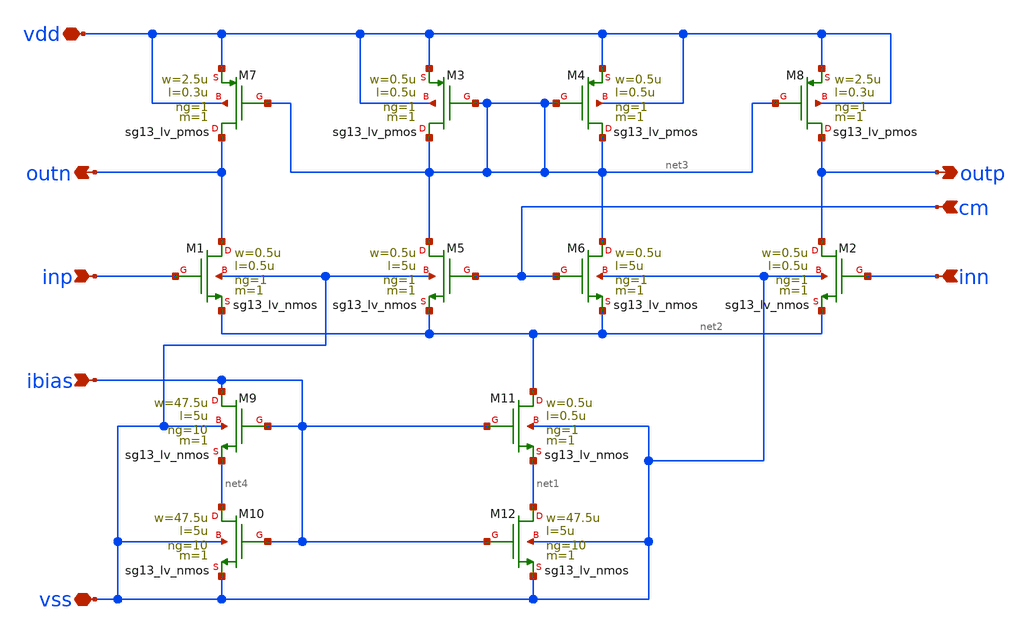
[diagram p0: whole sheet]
** sch_path: 3_Real_Cir/ota_gm_100u.sch
**.subckt ota_gm_100u inn outp outn vdd cm vss ibias inp
*.ipin inn
*.opin outp
*.opin outn
*.iopin vdd
*.ipin cm
*.iopin vss
*.ipin ibias
*.ipin inp
XM3 net3 net3 vdd vdd sg13_lv_pmos w=0.5u l=0.5u ng=1 m=1 mm_ok=1
XM4 net3 net3 vdd vdd sg13_lv_pmos w=0.5u l=0.5u ng=1 m=1 mm_ok=1
XM1 outn inp net2 vss sg13_lv_nmos w=0.5u l=0.5u ng=1 m=1 mm_ok=1
XM2 outp inn net2 vss sg13_lv_nmos w=0.5u l=0.5u ng=1 m=1 mm_ok=1
XM11 net2 ibias net1 vss sg13_lv_nmos w=0.5u l=0.5u ng=1 m=1 mm_ok=1
XM8 outp net3 vdd vdd sg13_lv_pmos w=2.5u l=0.3u ng=1 m=1 mm_ok=1
XM7 outn net3 vdd vdd sg13_lv_pmos w=2.5u l=0.3u ng=1 m=1 mm_ok=1
XM5 net3 cm net2 vss sg13_lv_nmos w=0.5u l=5u ng=1 m=1 mm_ok=1
XM6 net3 cm net2 vss sg13_lv_nmos w=0.5u l=5u ng=1 m=1 mm_ok=1
XM12 net1 ibias vss vss sg13_lv_nmos w=47.5u l=5u ng=10 m=1 mm_ok=1
XM9 ibias ibias net4 vss sg13_lv_nmos w=47.5u l=5u ng=10 m=1 mm_ok=1
XM10 net4 ibias vss vss sg13_lv_nmos w=47.5u l=5u ng=10 m=1 mm_ok=1
**.ends
.end
